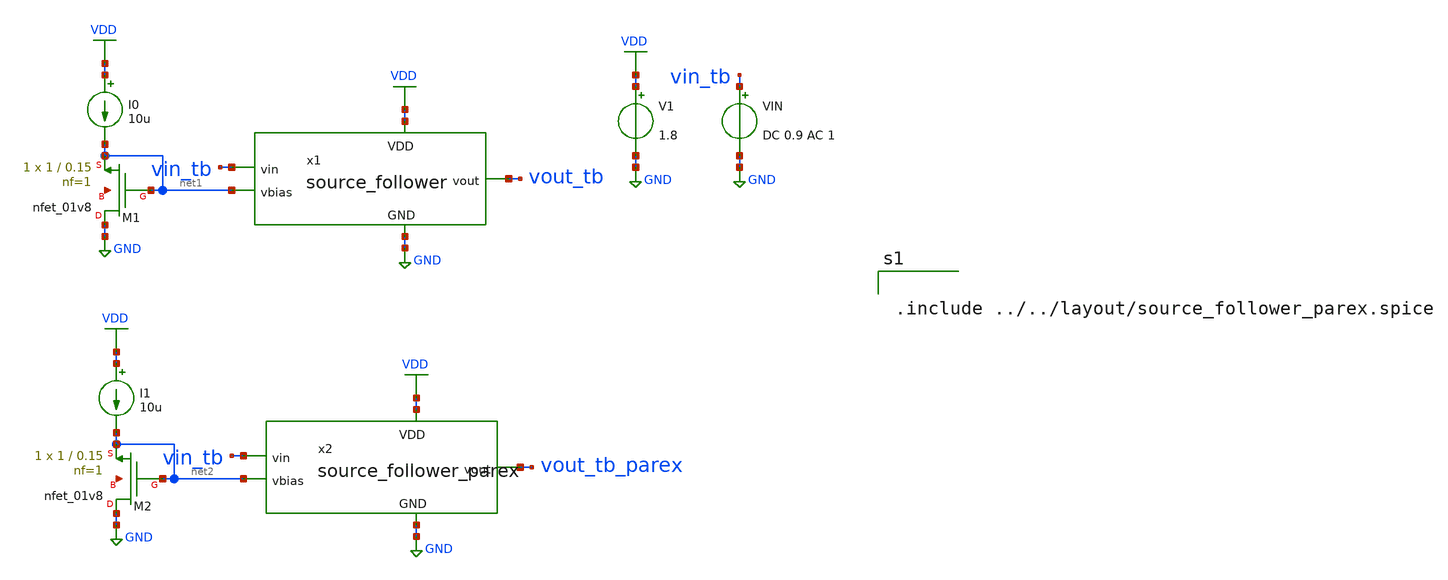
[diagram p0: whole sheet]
** sch_path: schematic/source_follower_tb_parex.sch
**.subckt source_follower_tb_parex
x1 VDD vin_tb vout_tb net1 GND source_follower
V1 VDD GND 1.8
VIN vin_tb GND DC 0.9 AC 1
XM1 GND net1 net1 net3 sky130_fd_pr__nfet_01v8 L=0.15 W=1 nf=1 ad='int((nf+1)/2) * W/nf * 0.29' as='int((nf+2)/2) * W/nf * 0.29'
+ pd='2*int((nf+1)/2) * (W/nf + 0.29)' ps='2*int((nf+2)/2) * (W/nf + 0.29)' nrd='0.29 / W' nrs='0.29 / W'
+ sa=0 sb=0 sd=0 mult=1 m=1
I0 VDD net1 10u
XM2 GND net2 net2 net4 sky130_fd_pr__nfet_01v8 L=0.15 W=1 nf=1 ad='int((nf+1)/2) * W/nf * 0.29' as='int((nf+2)/2) * W/nf * 0.29'
+ pd='2*int((nf+1)/2) * (W/nf + 0.29)' ps='2*int((nf+2)/2) * (W/nf + 0.29)' nrd='0.29 / W' nrs='0.29 / W'
+ sa=0 sb=0 sd=0 mult=1 m=1
I1 VDD net2 10u
x2 VDD vin_tb vout_tb_parex net2 GND source_follower_parex
**** begin user architecture code

** opencircuitdesign pdks install
.lib $::SKYWATER_MODELS/sky130.lib.spice tt




.include ../../layout/source_follower_parex.spice


**** end user architecture code
**.ends

* expanding   symbol:  source_follower.sym # of pins=5
** sym_path: schematic/source_follower.sym
** sch_path: schematic/source_follower.sch
.subckt source_follower VDD vin vout vbias GND
*.ipin GND
*.ipin vin
*.ipin vbias
*.ipin VDD
*.opin vout
XM1 VDD vin vout GND sky130_fd_pr__nfet_01v8 L=0.15 W=10 nf=1 ad='int((nf+1)/2) * W/nf * 0.29' as='int((nf+2)/2) * W/nf * 0.29'
+ pd='2*int((nf+1)/2) * (W/nf + 0.29)' ps='2*int((nf+2)/2) * (W/nf + 0.29)' nrd='0.29 / W' nrs='0.29 / W'
+ sa=0 sb=0 sd=0 mult=1 m=1
XM2 vout vbias GND GND sky130_fd_pr__nfet_01v8 L=0.15 W=1 nf=1 ad='int((nf+1)/2) * W/nf * 0.29' as='int((nf+2)/2) * W/nf * 0.29'
+ pd='2*int((nf+1)/2) * (W/nf + 0.29)' ps='2*int((nf+2)/2) * (W/nf + 0.29)' nrd='0.29 / W' nrs='0.29 / W'
+ sa=0 sb=0 sd=0 mult=1 m=1
.ends

.GLOBAL VDD
.GLOBAL GND
.end
